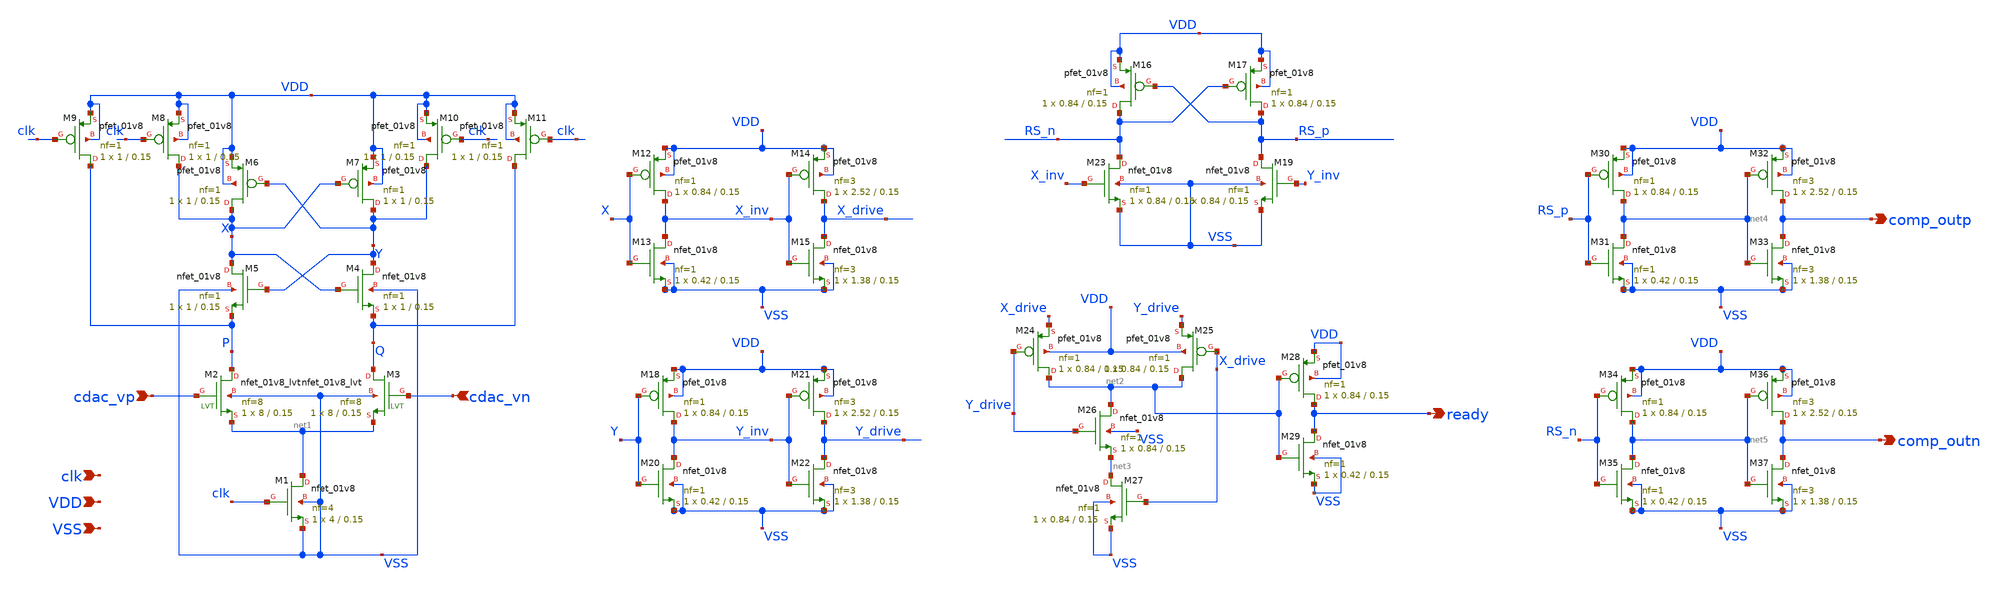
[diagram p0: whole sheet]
** sch_path: hgu/xschem/hgu_comp.sch
**.subckt hgu_comp cdac_vn cdac_vp VSS VDD clk ready comp_outp comp_outn
*.ipin cdac_vn
*.ipin cdac_vp
*.ipin VSS
*.ipin VDD
*.ipin clk
*.opin ready
*.opin comp_outp
*.opin comp_outn
XM1 net1 clk VSS VSS sky130_fd_pr__nfet_01v8 L=0.15 W=4 nf=4 ad='int((nf+1)/2) * W/nf * 0.29' as='int((nf+2)/2) * W/nf * 0.29'
+ pd='2*int((nf+1)/2) * (W/nf + 0.29)' ps='2*int((nf+2)/2) * (W/nf + 0.29)' nrd='0.29 / W' nrs='0.29 / W'
+ sa=0 sb=0 sd=0 mult=1 m=1
XM4 Y X Q VSS sky130_fd_pr__nfet_01v8 L=0.15 W=1 nf=1 ad='int((nf+1)/2) * W/nf * 0.29' as='int((nf+2)/2) * W/nf * 0.29'
+ pd='2*int((nf+1)/2) * (W/nf + 0.29)' ps='2*int((nf+2)/2) * (W/nf + 0.29)' nrd='0.29 / W' nrs='0.29 / W'
+ sa=0 sb=0 sd=0 mult=1 m=1
XM5 X Y P VSS sky130_fd_pr__nfet_01v8 L=0.15 W=1 nf=1 ad='int((nf+1)/2) * W/nf * 0.29' as='int((nf+2)/2) * W/nf * 0.29'
+ pd='2*int((nf+1)/2) * (W/nf + 0.29)' ps='2*int((nf+2)/2) * (W/nf + 0.29)' nrd='0.29 / W' nrs='0.29 / W'
+ sa=0 sb=0 sd=0 mult=1 m=1
XM6 X Y VDD VDD sky130_fd_pr__pfet_01v8 L=0.15 W=1 nf=1 ad='int((nf+1)/2) * W/nf * 0.29' as='int((nf+2)/2) * W/nf * 0.29'
+ pd='2*int((nf+1)/2) * (W/nf + 0.29)' ps='2*int((nf+2)/2) * (W/nf + 0.29)' nrd='0.29 / W' nrs='0.29 / W'
+ sa=0 sb=0 sd=0 mult=1 m=1
XM7 Y X VDD VDD sky130_fd_pr__pfet_01v8 L=0.15 W=1 nf=1 ad='int((nf+1)/2) * W/nf * 0.29' as='int((nf+2)/2) * W/nf * 0.29'
+ pd='2*int((nf+1)/2) * (W/nf + 0.29)' ps='2*int((nf+2)/2) * (W/nf + 0.29)' nrd='0.29 / W' nrs='0.29 / W'
+ sa=0 sb=0 sd=0 mult=1 m=1
XM8 X clk VDD VDD sky130_fd_pr__pfet_01v8 L=0.15 W=1 nf=1 ad='int((nf+1)/2) * W/nf * 0.29' as='int((nf+2)/2) * W/nf * 0.29'
+ pd='2*int((nf+1)/2) * (W/nf + 0.29)' ps='2*int((nf+2)/2) * (W/nf + 0.29)' nrd='0.29 / W' nrs='0.29 / W'
+ sa=0 sb=0 sd=0 mult=1 m=1
XM9 P clk VDD VDD sky130_fd_pr__pfet_01v8 L=0.15 W=1 nf=1 ad='int((nf+1)/2) * W/nf * 0.29' as='int((nf+2)/2) * W/nf * 0.29'
+ pd='2*int((nf+1)/2) * (W/nf + 0.29)' ps='2*int((nf+2)/2) * (W/nf + 0.29)' nrd='0.29 / W' nrs='0.29 / W'
+ sa=0 sb=0 sd=0 mult=1 m=1
XM10 Y clk VDD VDD sky130_fd_pr__pfet_01v8 L=0.15 W=1 nf=1 ad='int((nf+1)/2) * W/nf * 0.29' as='int((nf+2)/2) * W/nf * 0.29'
+ pd='2*int((nf+1)/2) * (W/nf + 0.29)' ps='2*int((nf+2)/2) * (W/nf + 0.29)' nrd='0.29 / W' nrs='0.29 / W'
+ sa=0 sb=0 sd=0 mult=1 m=1
XM11 Q clk VDD VDD sky130_fd_pr__pfet_01v8 L=0.15 W=1 nf=1 ad='int((nf+1)/2) * W/nf * 0.29' as='int((nf+2)/2) * W/nf * 0.29'
+ pd='2*int((nf+1)/2) * (W/nf + 0.29)' ps='2*int((nf+2)/2) * (W/nf + 0.29)' nrd='0.29 / W' nrs='0.29 / W'
+ sa=0 sb=0 sd=0 mult=1 m=1
XM16 RS_n RS_p VDD VDD sky130_fd_pr__pfet_01v8 L=0.15 W=0.84 nf=1 ad='int((nf+1)/2) * W/nf * 0.29' as='int((nf+2)/2) * W/nf * 0.29'
+ pd='2*int((nf+1)/2) * (W/nf + 0.29)' ps='2*int((nf+2)/2) * (W/nf + 0.29)' nrd='0.29 / W' nrs='0.29 / W'
+ sa=0 sb=0 sd=0 mult=1 m=1
XM17 RS_p RS_n VDD VDD sky130_fd_pr__pfet_01v8 L=0.15 W=0.84 nf=1 ad='int((nf+1)/2) * W/nf * 0.29' as='int((nf+2)/2) * W/nf * 0.29'
+ pd='2*int((nf+1)/2) * (W/nf + 0.29)' ps='2*int((nf+2)/2) * (W/nf + 0.29)' nrd='0.29 / W' nrs='0.29 / W'
+ sa=0 sb=0 sd=0 mult=1 m=1
XM19 RS_p Y_inv VSS VSS sky130_fd_pr__nfet_01v8 L=0.15 W=0.84 nf=1 ad='int((nf+1)/2) * W/nf * 0.29' as='int((nf+2)/2) * W/nf * 0.29'
+ pd='2*int((nf+1)/2) * (W/nf + 0.29)' ps='2*int((nf+2)/2) * (W/nf + 0.29)' nrd='0.29 / W' nrs='0.29 / W'
+ sa=0 sb=0 sd=0 mult=1 m=1
XM23 RS_n X_inv VSS VSS sky130_fd_pr__nfet_01v8 L=0.15 W=0.84 nf=1 ad='int((nf+1)/2) * W/nf * 0.29' as='int((nf+2)/2) * W/nf * 0.29'
+ pd='2*int((nf+1)/2) * (W/nf + 0.29)' ps='2*int((nf+2)/2) * (W/nf + 0.29)' nrd='0.29 / W' nrs='0.29 / W'
+ sa=0 sb=0 sd=0 mult=1 m=1
XM2 P cdac_vp net1 VSS sky130_fd_pr__nfet_01v8_lvt L=0.15 W=8 nf=8 ad='int((nf+1)/2) * W / nf * 0.29'
+ as='int((nf+2)/2) * W / nf * 0.29' pd='2*int((nf+1)/2) * (W / nf + 0.29)' ps='2*int((nf+2)/2) * (W / nf + 0.29)'
+ nrd='0.29 / W ' nrs='0.29 / W ' sa=0 sb=0 sd=0 mult=1 m=1
XM3 Q cdac_vn net1 VSS sky130_fd_pr__nfet_01v8_lvt L=0.15 W=8 nf=8 ad='int((nf+1)/2) * W / nf * 0.29'
+ as='int((nf+2)/2) * W / nf * 0.29' pd='2*int((nf+1)/2) * (W / nf + 0.29)' ps='2*int((nf+2)/2) * (W / nf + 0.29)'
+ nrd='0.29 / W ' nrs='0.29 / W ' sa=0 sb=0 sd=0 mult=1 m=1
XM12 X_inv X VDD VDD sky130_fd_pr__pfet_01v8 L=0.15 W=0.84 nf=1 ad='int((nf+1)/2) * W/nf * 0.29' as='int((nf+2)/2) * W/nf * 0.29'
+ pd='2*int((nf+1)/2) * (W/nf + 0.29)' ps='2*int((nf+2)/2) * (W/nf + 0.29)' nrd='0.29 / W' nrs='0.29 / W'
+ sa=0 sb=0 sd=0 mult=1 m=1
XM13 X_inv X VSS VSS sky130_fd_pr__nfet_01v8 L=0.15 W=0.42 nf=1 ad='int((nf+1)/2) * W/nf * 0.29' as='int((nf+2)/2) * W/nf * 0.29'
+ pd='2*int((nf+1)/2) * (W/nf + 0.29)' ps='2*int((nf+2)/2) * (W/nf + 0.29)' nrd='0.29 / W' nrs='0.29 / W'
+ sa=0 sb=0 sd=0 mult=1 m=1
XM14 X_drive X_inv VDD VDD sky130_fd_pr__pfet_01v8 L=0.15 W=2.52 nf=3 ad='int((nf+1)/2) * W/nf * 0.29'
+ as='int((nf+2)/2) * W/nf * 0.29' pd='2*int((nf+1)/2) * (W/nf + 0.29)' ps='2*int((nf+2)/2) * (W/nf + 0.29)'
+ nrd='0.29 / W' nrs='0.29 / W' sa=0 sb=0 sd=0 mult=1 m=1
XM15 X_drive X_inv VSS VSS sky130_fd_pr__nfet_01v8 L=0.15 W=1.38 nf=3 ad='int((nf+1)/2) * W/nf * 0.29'
+ as='int((nf+2)/2) * W/nf * 0.29' pd='2*int((nf+1)/2) * (W/nf + 0.29)' ps='2*int((nf+2)/2) * (W/nf + 0.29)'
+ nrd='0.29 / W' nrs='0.29 / W' sa=0 sb=0 sd=0 mult=1 m=1
XM18 Y_inv Y VDD VDD sky130_fd_pr__pfet_01v8 L=0.15 W=0.84 nf=1 ad='int((nf+1)/2) * W/nf * 0.29' as='int((nf+2)/2) * W/nf * 0.29'
+ pd='2*int((nf+1)/2) * (W/nf + 0.29)' ps='2*int((nf+2)/2) * (W/nf + 0.29)' nrd='0.29 / W' nrs='0.29 / W'
+ sa=0 sb=0 sd=0 mult=1 m=1
XM20 Y_inv Y VSS VSS sky130_fd_pr__nfet_01v8 L=0.15 W=0.42 nf=1 ad='int((nf+1)/2) * W/nf * 0.29' as='int((nf+2)/2) * W/nf * 0.29'
+ pd='2*int((nf+1)/2) * (W/nf + 0.29)' ps='2*int((nf+2)/2) * (W/nf + 0.29)' nrd='0.29 / W' nrs='0.29 / W'
+ sa=0 sb=0 sd=0 mult=1 m=1
XM21 Y_drive Y_inv VDD VDD sky130_fd_pr__pfet_01v8 L=0.15 W=2.52 nf=3 ad='int((nf+1)/2) * W/nf * 0.29'
+ as='int((nf+2)/2) * W/nf * 0.29' pd='2*int((nf+1)/2) * (W/nf + 0.29)' ps='2*int((nf+2)/2) * (W/nf + 0.29)'
+ nrd='0.29 / W' nrs='0.29 / W' sa=0 sb=0 sd=0 mult=1 m=1
XM22 Y_drive Y_inv VSS VSS sky130_fd_pr__nfet_01v8 L=0.15 W=1.38 nf=3 ad='int((nf+1)/2) * W/nf * 0.29'
+ as='int((nf+2)/2) * W/nf * 0.29' pd='2*int((nf+1)/2) * (W/nf + 0.29)' ps='2*int((nf+2)/2) * (W/nf + 0.29)'
+ nrd='0.29 / W' nrs='0.29 / W' sa=0 sb=0 sd=0 mult=1 m=1
XM24 net2 Y_drive X_drive VDD sky130_fd_pr__pfet_01v8 L=0.15 W=0.84 nf=1 ad='int((nf+1)/2) * W/nf * 0.29'
+ as='int((nf+2)/2) * W/nf * 0.29' pd='2*int((nf+1)/2) * (W/nf + 0.29)' ps='2*int((nf+2)/2) * (W/nf + 0.29)'
+ nrd='0.29 / W' nrs='0.29 / W' sa=0 sb=0 sd=0 mult=1 m=1
XM25 net2 X_drive Y_drive VDD sky130_fd_pr__pfet_01v8 L=0.15 W=0.84 nf=1 ad='int((nf+1)/2) * W/nf * 0.29'
+ as='int((nf+2)/2) * W/nf * 0.29' pd='2*int((nf+1)/2) * (W/nf + 0.29)' ps='2*int((nf+2)/2) * (W/nf + 0.29)'
+ nrd='0.29 / W' nrs='0.29 / W' sa=0 sb=0 sd=0 mult=1 m=1
XM26 net2 Y_drive net3 VSS sky130_fd_pr__nfet_01v8 L=0.15 W=0.84 nf=1 ad='int((nf+1)/2) * W/nf * 0.29'
+ as='int((nf+2)/2) * W/nf * 0.29' pd='2*int((nf+1)/2) * (W/nf + 0.29)' ps='2*int((nf+2)/2) * (W/nf + 0.29)'
+ nrd='0.29 / W' nrs='0.29 / W' sa=0 sb=0 sd=0 mult=1 m=1
XM27 net3 X_drive VSS VSS sky130_fd_pr__nfet_01v8 L=0.15 W=0.84 nf=1 ad='int((nf+1)/2) * W/nf * 0.29'
+ as='int((nf+2)/2) * W/nf * 0.29' pd='2*int((nf+1)/2) * (W/nf + 0.29)' ps='2*int((nf+2)/2) * (W/nf + 0.29)'
+ nrd='0.29 / W' nrs='0.29 / W' sa=0 sb=0 sd=0 mult=1 m=1
XM28 ready net2 VDD VDD sky130_fd_pr__pfet_01v8 L=0.15 W=0.84 nf=1 ad='int((nf+1)/2) * W/nf * 0.29' as='int((nf+2)/2) * W/nf * 0.29'
+ pd='2*int((nf+1)/2) * (W/nf + 0.29)' ps='2*int((nf+2)/2) * (W/nf + 0.29)' nrd='0.29 / W' nrs='0.29 / W'
+ sa=0 sb=0 sd=0 mult=1 m=1
XM29 ready net2 VSS VSS sky130_fd_pr__nfet_01v8 L=0.15 W=0.42 nf=1 ad='int((nf+1)/2) * W/nf * 0.29' as='int((nf+2)/2) * W/nf * 0.29'
+ pd='2*int((nf+1)/2) * (W/nf + 0.29)' ps='2*int((nf+2)/2) * (W/nf + 0.29)' nrd='0.29 / W' nrs='0.29 / W'
+ sa=0 sb=0 sd=0 mult=1 m=1
XM30 net4 RS_p VDD VDD sky130_fd_pr__pfet_01v8 L=0.15 W=0.84 nf=1 ad='int((nf+1)/2) * W/nf * 0.29' as='int((nf+2)/2) * W/nf * 0.29'
+ pd='2*int((nf+1)/2) * (W/nf + 0.29)' ps='2*int((nf+2)/2) * (W/nf + 0.29)' nrd='0.29 / W' nrs='0.29 / W'
+ sa=0 sb=0 sd=0 mult=1 m=1
XM31 net4 RS_p VSS VSS sky130_fd_pr__nfet_01v8 L=0.15 W=0.42 nf=1 ad='int((nf+1)/2) * W/nf * 0.29' as='int((nf+2)/2) * W/nf * 0.29'
+ pd='2*int((nf+1)/2) * (W/nf + 0.29)' ps='2*int((nf+2)/2) * (W/nf + 0.29)' nrd='0.29 / W' nrs='0.29 / W'
+ sa=0 sb=0 sd=0 mult=1 m=1
XM32 comp_outp net4 VDD VDD sky130_fd_pr__pfet_01v8 L=0.15 W=2.52 nf=3 ad='int((nf+1)/2) * W/nf * 0.29'
+ as='int((nf+2)/2) * W/nf * 0.29' pd='2*int((nf+1)/2) * (W/nf + 0.29)' ps='2*int((nf+2)/2) * (W/nf + 0.29)'
+ nrd='0.29 / W' nrs='0.29 / W' sa=0 sb=0 sd=0 mult=1 m=1
XM33 comp_outp net4 VSS VSS sky130_fd_pr__nfet_01v8 L=0.15 W=1.38 nf=3 ad='int((nf+1)/2) * W/nf * 0.29'
+ as='int((nf+2)/2) * W/nf * 0.29' pd='2*int((nf+1)/2) * (W/nf + 0.29)' ps='2*int((nf+2)/2) * (W/nf + 0.29)'
+ nrd='0.29 / W' nrs='0.29 / W' sa=0 sb=0 sd=0 mult=1 m=1
XM34 net5 RS_n VDD VDD sky130_fd_pr__pfet_01v8 L=0.15 W=0.84 nf=1 ad='int((nf+1)/2) * W/nf * 0.29' as='int((nf+2)/2) * W/nf * 0.29'
+ pd='2*int((nf+1)/2) * (W/nf + 0.29)' ps='2*int((nf+2)/2) * (W/nf + 0.29)' nrd='0.29 / W' nrs='0.29 / W'
+ sa=0 sb=0 sd=0 mult=1 m=1
XM35 net5 RS_n VSS VSS sky130_fd_pr__nfet_01v8 L=0.15 W=0.42 nf=1 ad='int((nf+1)/2) * W/nf * 0.29' as='int((nf+2)/2) * W/nf * 0.29'
+ pd='2*int((nf+1)/2) * (W/nf + 0.29)' ps='2*int((nf+2)/2) * (W/nf + 0.29)' nrd='0.29 / W' nrs='0.29 / W'
+ sa=0 sb=0 sd=0 mult=1 m=1
XM36 comp_outn net5 VDD VDD sky130_fd_pr__pfet_01v8 L=0.15 W=2.52 nf=3 ad='int((nf+1)/2) * W/nf * 0.29'
+ as='int((nf+2)/2) * W/nf * 0.29' pd='2*int((nf+1)/2) * (W/nf + 0.29)' ps='2*int((nf+2)/2) * (W/nf + 0.29)'
+ nrd='0.29 / W' nrs='0.29 / W' sa=0 sb=0 sd=0 mult=1 m=1
XM37 comp_outn net5 VSS VSS sky130_fd_pr__nfet_01v8 L=0.15 W=1.38 nf=3 ad='int((nf+1)/2) * W/nf * 0.29'
+ as='int((nf+2)/2) * W/nf * 0.29' pd='2*int((nf+1)/2) * (W/nf + 0.29)' ps='2*int((nf+2)/2) * (W/nf + 0.29)'
+ nrd='0.29 / W' nrs='0.29 / W' sa=0 sb=0 sd=0 mult=1 m=1
**.ends
.end
